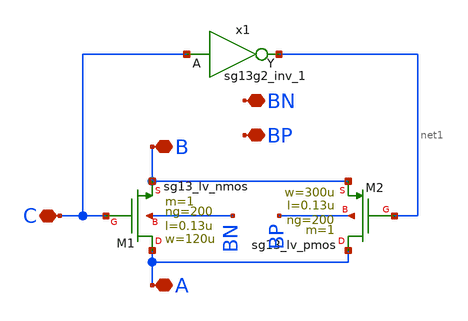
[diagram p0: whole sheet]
** sch_path: src/analog/tg/tg.sch
**.subckt tg B A BN BP C
*.iopin B
*.iopin A
*.iopin BN
*.iopin BP
*.iopin C
XM1 A C B BN sg13_lv_nmos w=120u l=0.13u ng=200 m=1 mm_ok=1
XM2 A net1 B BP sg13_lv_pmos w=300u l=0.13u ng=200 m=1 mm_ok=1
x1 net1 C BP BN sg13g2_inv_1
**.ends

* expanding   symbol:  sg13g2_stdcells/sg13g2_inv_1.sym # of pins=2
** sym_path: sg13g2_stdcells/sg13g2_inv_1.sym
** sch_path: sg13g2_stdcells/sg13g2_inv_1.sch
.subckt sg13g2_inv_1 Y A VDD VSS
*.opin Y
*.ipin A
*.iopin VDD
*.iopin VSS
XM1 Y A VSS VSS sg13_lv_nmos w=740.00n l=130.00n ng=1 m=1 mm_ok=1
XM2 Y A VDD VDD sg13_lv_pmos w=1.12u l=130.00n ng=1 m=1 mm_ok=1
.ends

.end
